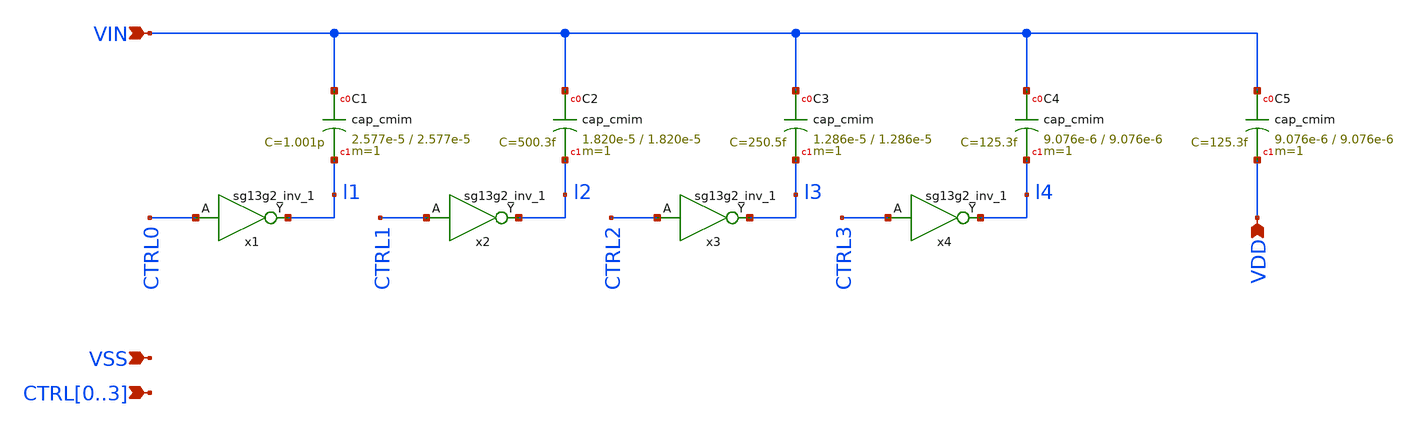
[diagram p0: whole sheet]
** sch_path: designs/cdac/cdac.sch
**.subckt cdac VIN CTRL0,CTRL1,CTRL2,CTRL3 VDD VSS
*.ipin VIN
*.ipin CTRL0,CTRL1,CTRL2,CTRL3
*.ipin VDD
*.ipin VSS
XC1 VIN l1 cap_cmim w=2.577e-5 l=2.577e-5 m=1 mm_ok=1
XC2 VIN l2 cap_cmim w=1.820e-5 l=1.820e-5 m=1 mm_ok=1
XC3 VIN l3 cap_cmim w=1.286e-5 l=1.286e-5 m=1 mm_ok=1
XC4 VIN l4 cap_cmim w=9.076e-6 l=9.076e-6 m=1 mm_ok=1
x1 l1 CTRL0 VDD VSS sg13g2_inv_1
x2 l2 CTRL1 VDD VSS sg13g2_inv_1
x3 l3 CTRL2 VDD VSS sg13g2_inv_1
x4 l4 CTRL3 VDD VSS sg13g2_inv_1
XC5 VIN VDD cap_cmim w=9.076e-6 l=9.076e-6 m=1 mm_ok=1
**.ends

* expanding   symbol:  sg13g2_stdcells/sg13g2_inv_1.sym # of pins=2
** sym_path: sg13g2_stdcells/sg13g2_inv_1.sym
** sch_path: sg13g2_stdcells/sg13g2_inv_1.sch
.subckt sg13g2_inv_1 Y A VDD VSS
*.opin Y
*.ipin A
*.iopin VDD
*.iopin VSS
XM1 Y A VSS VSS sg13_lv_nmos w=740.00n l=130.00n ng=1 m=1 mm_ok=1
XM2 Y A VDD VDD sg13_lv_pmos w=1.12u l=130.00n ng=1 m=1 mm_ok=1
.ends

.end
